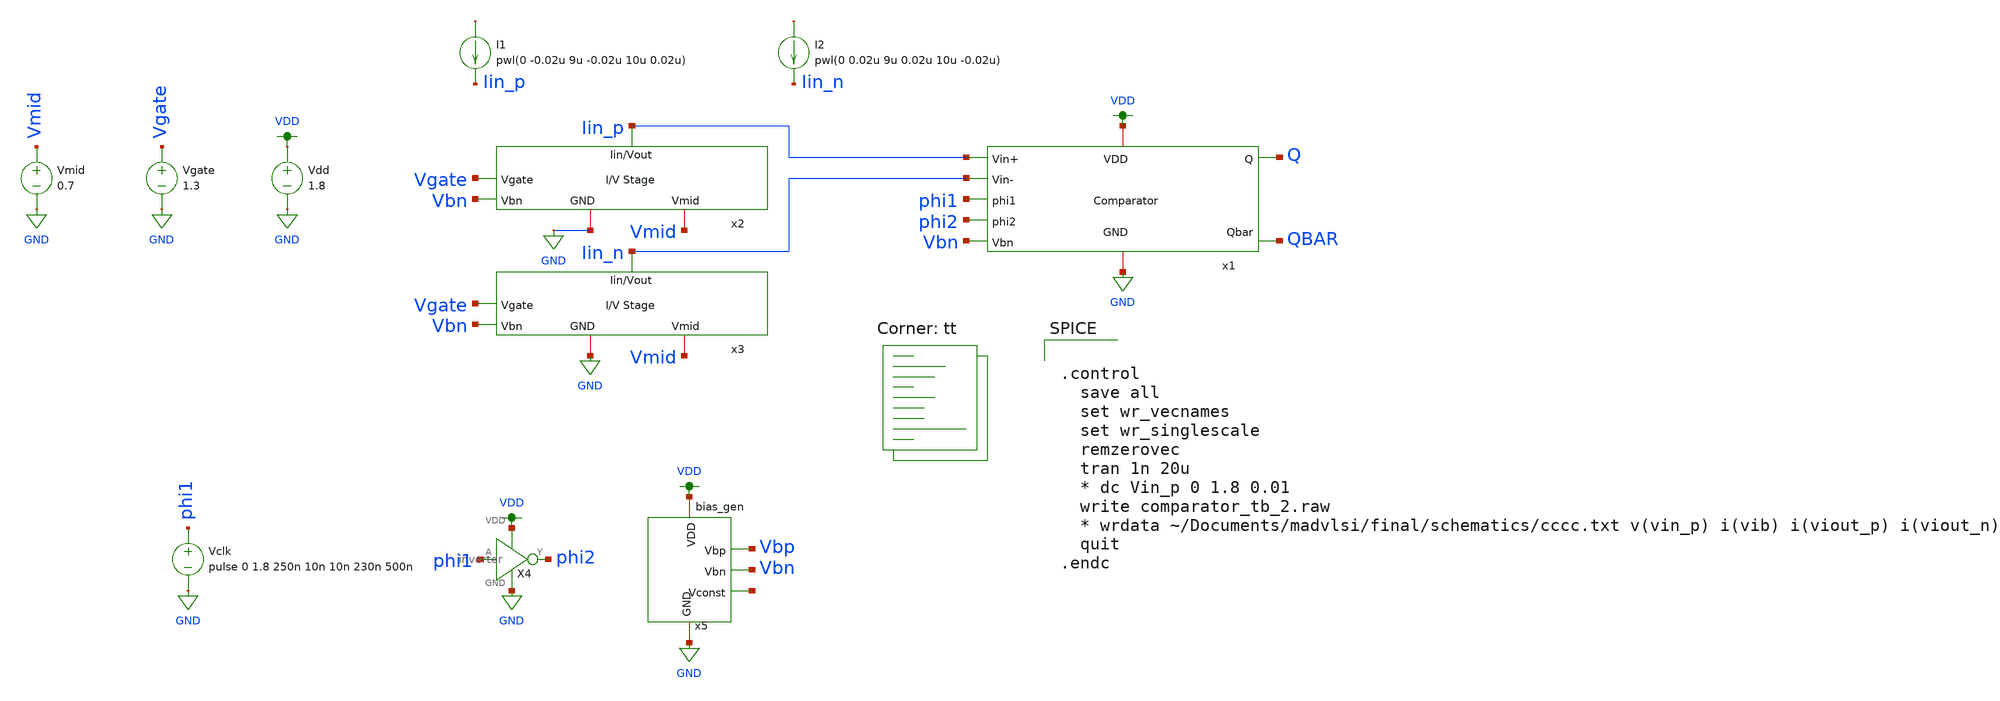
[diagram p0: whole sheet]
** sch_path: final/schematics/comparator_tb_2.sch
**.subckt comparator_tb_2
x1 VDD Vbn Iin_p Iin_n phi1 phi2 Q QBAR GND comparator
x2 Iin_p Vgate Vmid Vbn GND IV_converter
x3 Iin_n Vgate Vmid Vbn GND IV_converter
Vdd VDD GND 1.8
X4 VDD phi1 phi2 GND inverter
Vclk phi1 GND pulse 0 1.8 250n 10n 10n 230n 500n
I1 net1 Iin_p pwl(0 -0.02u 9u -0.02u 10u 0.02u)
I2 net2 Iin_n pwl(0 0.02u 9u 0.02u 10u -0.02u)
Vgate Vgate GND 1.3
Vmid Vmid GND 0.7
x5 VDD Vbp net3 GND Vbn bias_gen
**** begin user architecture code
.lib $::SKYWATER_MODELS/sky130.lib.spice tt


.control
  save all
  set wr_vecnames
  set wr_singlescale
  remzerovec
  tran 1n 20u
  * dc Vin_p 0 1.8 0.01
  write comparator_tb_2.raw
  * wrdata ~/Documents/madvlsi/final/schematics/cccc.txt v(vin_p) i(vib) i(viout_p) i(viout_n)
  quit
.endc


**** end user architecture code
**.ends

* expanding   symbol:  comparator.sym # of pins=9
** sym_path: final/schematics/comparator.sym
** sch_path: final/schematics/comparator.sch
.subckt comparator VDD Vbn Vin+ Vin- phi1 phi2 Q Qbar GND
*.ipin Vin+
*.ipin Vin-
*.ipin Vbn
*.ipin phi1
*.ipin phi2
*.opin Q
*.opin Qbar
*.iopin VDD
*.iopin GND
XM1 net2 Vin- net1 GND sky130_fd_pr__nfet_01v8 L=0.15 W=1 nf=1 ad='int((nf+1)/2) * W/nf * 0.29' as='int((nf+2)/2) * W/nf * 0.29'
+ pd='2*int((nf+1)/2) * (W/nf + 0.29)' ps='2*int((nf+2)/2) * (W/nf + 0.29)' nrd='0.29 / W' nrs='0.29 / W'
+ sa=0 sb=0 sd=0 mult=1 m=1
XM2 net1 Vin+ net3 GND sky130_fd_pr__nfet_01v8 L=0.15 W=1 nf=1 ad='int((nf+1)/2) * W/nf * 0.29' as='int((nf+2)/2) * W/nf * 0.29'
+ pd='2*int((nf+1)/2) * (W/nf + 0.29)' ps='2*int((nf+2)/2) * (W/nf + 0.29)' nrd='0.29 / W' nrs='0.29 / W'
+ sa=0 sb=0 sd=0 mult=1 m=1
XM3 VDD net3 net2 VDD sky130_fd_pr__pfet_01v8 L=0.15 W=1 nf=1 ad='int((nf+1)/2) * W/nf * 0.29' as='int((nf+2)/2) * W/nf * 0.29'
+ pd='2*int((nf+1)/2) * (W/nf + 0.29)' ps='2*int((nf+2)/2) * (W/nf + 0.29)' nrd='0.29 / W' nrs='0.29 / W'
+ sa=0 sb=0 sd=0 mult=1 m=1
XM4 net3 net2 VDD VDD sky130_fd_pr__pfet_01v8 L=0.15 W=1 nf=1 ad='int((nf+1)/2) * W/nf * 0.29' as='int((nf+2)/2) * W/nf * 0.29'
+ pd='2*int((nf+1)/2) * (W/nf + 0.29)' ps='2*int((nf+2)/2) * (W/nf + 0.29)' nrd='0.29 / W' nrs='0.29 / W'
+ sa=0 sb=0 sd=0 mult=1 m=1
XM5 net2 phi2 Q VDD sky130_fd_pr__pfet_01v8 L=0.15 W=1 nf=1 ad='int((nf+1)/2) * W/nf * 0.29' as='int((nf+2)/2) * W/nf * 0.29'
+ pd='2*int((nf+1)/2) * (W/nf + 0.29)' ps='2*int((nf+2)/2) * (W/nf + 0.29)' nrd='0.29 / W' nrs='0.29 / W'
+ sa=0 sb=0 sd=0 mult=1 m=1
XM6 Qbar phi2 net3 VDD sky130_fd_pr__pfet_01v8 L=0.15 W=1 nf=1 ad='int((nf+1)/2) * W/nf * 0.29' as='int((nf+2)/2) * W/nf * 0.29'
+ pd='2*int((nf+1)/2) * (W/nf + 0.29)' ps='2*int((nf+2)/2) * (W/nf + 0.29)' nrd='0.29 / W' nrs='0.29 / W'
+ sa=0 sb=0 sd=0 mult=1 m=1
XM7 net2 phi1 net3 VDD sky130_fd_pr__pfet_01v8 L=0.15 W=1 nf=1 ad='int((nf+1)/2) * W/nf * 0.29' as='int((nf+2)/2) * W/nf * 0.29'
+ pd='2*int((nf+1)/2) * (W/nf + 0.29)' ps='2*int((nf+2)/2) * (W/nf + 0.29)' nrd='0.29 / W' nrs='0.29 / W'
+ sa=0 sb=0 sd=0 mult=1 m=1
XM8 Qbar Q GND GND sky130_fd_pr__nfet_01v8 L=0.15 W=1 nf=1 ad='int((nf+1)/2) * W/nf * 0.29' as='int((nf+2)/2) * W/nf * 0.29'
+ pd='2*int((nf+1)/2) * (W/nf + 0.29)' ps='2*int((nf+2)/2) * (W/nf + 0.29)' nrd='0.29 / W' nrs='0.29 / W'
+ sa=0 sb=0 sd=0 mult=1 m=1
XM9 GND phi2 Qbar GND sky130_fd_pr__nfet_01v8 L=0.15 W=1 nf=1 ad='int((nf+1)/2) * W/nf * 0.29' as='int((nf+2)/2) * W/nf * 0.29'
+ pd='2*int((nf+1)/2) * (W/nf + 0.29)' ps='2*int((nf+2)/2) * (W/nf + 0.29)' nrd='0.29 / W' nrs='0.29 / W'
+ sa=0 sb=0 sd=0 mult=1 m=1
XM10 Q phi2 GND GND sky130_fd_pr__nfet_01v8 L=0.15 W=1 nf=1 ad='int((nf+1)/2) * W/nf * 0.29' as='int((nf+2)/2) * W/nf * 0.29'
+ pd='2*int((nf+1)/2) * (W/nf + 0.29)' ps='2*int((nf+2)/2) * (W/nf + 0.29)' nrd='0.29 / W' nrs='0.29 / W'
+ sa=0 sb=0 sd=0 mult=1 m=1
XM11 GND Qbar Q GND sky130_fd_pr__nfet_01v8 L=0.15 W=1 nf=1 ad='int((nf+1)/2) * W/nf * 0.29' as='int((nf+2)/2) * W/nf * 0.29'
+ pd='2*int((nf+1)/2) * (W/nf + 0.29)' ps='2*int((nf+2)/2) * (W/nf + 0.29)' nrd='0.29 / W' nrs='0.29 / W'
+ sa=0 sb=0 sd=0 mult=1 m=1
XM12 GND Vbn net1 GND sky130_fd_pr__nfet_01v8 L=0.15 W=1 nf=1 ad='int((nf+1)/2) * W/nf * 0.29' as='int((nf+2)/2) * W/nf * 0.29'
+ pd='2*int((nf+1)/2) * (W/nf + 0.29)' ps='2*int((nf+2)/2) * (W/nf + 0.29)' nrd='0.29 / W' nrs='0.29 / W'
+ sa=0 sb=0 sd=0 mult=1 m=1
.ends


* expanding   symbol:  IV_converter.sym # of pins=5
** sym_path: final/schematics/IV_converter.sym
** sch_path: final/schematics/IV_converter.sch
.subckt IV_converter Iin_Vout Vgate Vmid Vbn GND
*.iopin Iin_Vout
*.iopin GND
*.iopin Vmid
*.ipin Vbn
*.ipin Vgate
XM1 GND net1 Iin_Vout VDD sky130_fd_pr__pfet_01v8 L={len} W={wid} nf=1 ad='int((nf+1)/2) * W/nf * 0.29'
+ as='int((nf+2)/2) * W/nf * 0.29' pd='2*int((nf+1)/2) * (W/nf + 0.29)' ps='2*int((nf+2)/2) * (W/nf + 0.29)'
+ nrd='0.29 / W' nrs='0.29 / W' sa=0 sb=0 sd=0 mult=1 m=1
XM2 net1 net1 Vmid Vmid sky130_fd_pr__pfet_01v8 L={len} W={wid} nf=1 ad='int((nf+1)/2) * W/nf * 0.29'
+ as='int((nf+2)/2) * W/nf * 0.29' pd='2*int((nf+1)/2) * (W/nf + 0.29)' ps='2*int((nf+2)/2) * (W/nf + 0.29)'
+ nrd='0.29 / W' nrs='0.29 / W' sa=0 sb=0 sd=0 mult=1 m=1
XM3 net1 Vbn GND GND sky130_fd_pr__nfet_01v8 L={len} W={wid} nf=1 ad='int((nf+1)/2) * W/nf * 0.29' as='int((nf+2)/2) * W/nf * 0.29'
+ pd='2*int((nf+1)/2) * (W/nf + 0.29)' ps='2*int((nf+2)/2) * (W/nf + 0.29)' nrd='0.29 / W' nrs='0.29 / W'
+ sa=0 sb=0 sd=0 mult=1 m=1
XM4 Iin_Vout Vgate Vmid GND sky130_fd_pr__nfet_01v8 L=4 W=1 nf=1 ad='int((nf+1)/2) * W/nf * 0.29' as='int((nf+2)/2) * W/nf * 0.29'
+ pd='2*int((nf+1)/2) * (W/nf + 0.29)' ps='2*int((nf+2)/2) * (W/nf + 0.29)' nrd='0.29 / W' nrs='0.29 / W'
+ sa=0 sb=0 sd=0 mult=1 m=1
**** begin user architecture code


.param wid=3 len=0.5


**** end user architecture code
.ends


* expanding   symbol:  inverter.sym # of pins=4
** sym_path: final/schematics/inverter.sym
** sch_path: final/schematics/inverter.sch
.subckt inverter VDD A Y GND
*.ipin A
*.iopin VDD
*.iopin GND
*.opin Y
XM1 Y A GND GND sky130_fd_pr__nfet_01v8 L={len} W={wid} nf=1 ad='int((nf+1)/2) * W/nf * 0.29' as='int((nf+2)/2) * W/nf * 0.29'
+ pd='2*int((nf+1)/2) * (W/nf + 0.29)' ps='2*int((nf+2)/2) * (W/nf + 0.29)' nrd='0.29 / W' nrs='0.29 / W'
+ sa=0 sb=0 sd=0 mult=1 m=1
XM2 Y A VDD VDD sky130_fd_pr__pfet_01v8 L={len} W={wid} nf=1 ad='int((nf+1)/2) * W/nf * 0.29' as='int((nf+2)/2) * W/nf * 0.29'
+ pd='2*int((nf+1)/2) * (W/nf + 0.29)' ps='2*int((nf+2)/2) * (W/nf + 0.29)' nrd='0.29 / W' nrs='0.29 / W'
+ sa=0 sb=0 sd=0 mult=1 m=1
**** begin user architecture code


.param wid=3 len=0.5


**** end user architecture code
.ends


* expanding   symbol:  /home/madvlsi/Documents/madvlsi/final/schematics/bias_gen/bias_gen.sym # of
*+ pins=5
** sym_path: final/schematics/bias_gen/bias_gen.sym
** sch_path: final/schematics/bias_gen/bias_gen.sch
.subckt bias_gen VDD Vbp Vconst GND Vbn
*.iopin VDD
*.opin Vbp
*.iopin GND
*.opin Vbn
*.opin Vconst
**** begin user architecture code

.param len=0.5 wid=3

**** end user architecture code
XM10 Vconst net1 net1 GND sky130_fd_pr__nfet_01v8 L={len} W={wid} nf=1 ad='int((nf+1)/2) * W/nf * 0.29'
+ as='int((nf+2)/2) * W/nf * 0.29' pd='2*int((nf+1)/2) * (W/nf + 0.29)' ps='2*int((nf+2)/2) * (W/nf + 0.29)'
+ nrd='0.29 / W' nrs='0.29 / W' sa=0 sb=0 sd=0 mult=10 m=10
XM11 Vbn Vbn GND GND sky130_fd_pr__nfet_01v8 L={len} W={wid} nf=1 ad='int((nf+1)/2) * W/nf * 0.29' as='int((nf+2)/2) * W/nf * 0.29'
+ pd='2*int((nf+1)/2) * (W/nf + 0.29)' ps='2*int((nf+2)/2) * (W/nf + 0.29)' nrd='0.29 / W' nrs='0.29 / W'
+ sa=0 sb=0 sd=0 mult=1 m=1
XM12 GND Vbp GND GND sky130_fd_pr__nfet_01v8 L=10 W=10 nf=1 ad='int((nf+1)/2) * W/nf * 0.29' as='int((nf+2)/2) * W/nf * 0.29'
+ pd='2*int((nf+1)/2) * (W/nf + 0.29)' ps='2*int((nf+2)/2) * (W/nf + 0.29)' nrd='0.29 / W' nrs='0.29 / W'
+ sa=0 sb=0 sd=0 mult=1 m=1
XM13 VDD Vbp net1 VDD sky130_fd_pr__pfet_01v8 L={len} W={wid} nf=1 ad='int((nf+1)/2) * W/nf * 0.29' as='int((nf+2)/2) * W/nf * 0.29'
+ pd='2*int((nf+1)/2) * (W/nf + 0.29)' ps='2*int((nf+2)/2) * (W/nf + 0.29)' nrd='0.29 / W' nrs='0.29 / W'
+ sa=0 sb=0 sd=0 mult=1 m=1
XM14 GND Vbn Vbp GND sky130_fd_pr__nfet_01v8 L={len} W={wid} nf=1 ad='int((nf+1)/2) * W/nf * 0.29' as='int((nf+2)/2) * W/nf * 0.29'
+ pd='2*int((nf+1)/2) * (W/nf + 0.29)' ps='2*int((nf+2)/2) * (W/nf + 0.29)' nrd='0.29 / W' nrs='0.29 / W'
+ sa=0 sb=0 sd=0 mult=1 m=1
XM15 net2 net1 GND GND sky130_fd_pr__nfet_01v8 L={len} W={wid} nf=1 ad='int((nf+1)/2) * W/nf * 0.29'
+ as='int((nf+2)/2) * W/nf * 0.29' pd='2*int((nf+1)/2) * (W/nf + 0.29)' ps='2*int((nf+2)/2) * (W/nf + 0.29)'
+ nrd='0.29 / W' nrs='0.29 / W' sa=0 sb=0 sd=0 mult=1 m=1
XM16 VDD net2 net2 VDD sky130_fd_pr__pfet_01v8 L={len} W={wid} nf=1 ad='int((nf+1)/2) * W/nf * 0.29'
+ as='int((nf+2)/2) * W/nf * 0.29' pd='2*int((nf+1)/2) * (W/nf + 0.29)' ps='2*int((nf+2)/2) * (W/nf + 0.29)'
+ nrd='0.29 / W' nrs='0.29 / W' sa=0 sb=0 sd=0 mult=1 m=1
XM17 Vbp net2 VDD VDD sky130_fd_pr__pfet_01v8 L={len} W={wid} nf=1 ad='int((nf+1)/2) * W/nf * 0.29' as='int((nf+2)/2) * W/nf * 0.29'
+ pd='2*int((nf+1)/2) * (W/nf + 0.29)' ps='2*int((nf+2)/2) * (W/nf + 0.29)' nrd='0.29 / W' nrs='0.29 / W'
+ sa=0 sb=0 sd=0 mult=1 m=1
XM18 Vbn Vbp VDD VDD sky130_fd_pr__pfet_01v8 L={len} W={wid} nf=1 ad='int((nf+1)/2) * W/nf * 0.29' as='int((nf+2)/2) * W/nf * 0.29'
+ pd='2*int((nf+1)/2) * (W/nf + 0.29)' ps='2*int((nf+2)/2) * (W/nf + 0.29)' nrd='0.29 / W' nrs='0.29 / W'
+ sa=0 sb=0 sd=0 mult=1 m=1
XR2 GND Vconst GND sky130_fd_pr__res_high_po_0p35 L=9 mult=1 m=1
.ends

.GLOBAL GND
.GLOBAL VDD
.end
